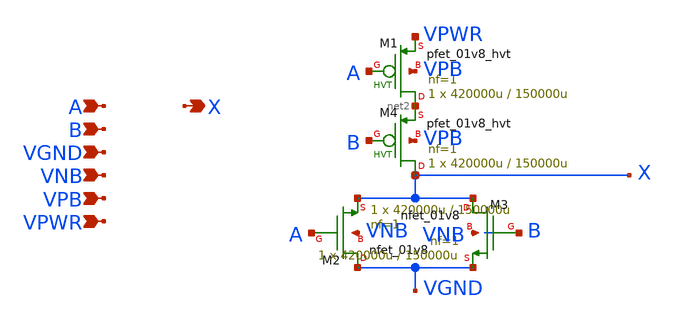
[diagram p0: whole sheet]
** sch_path: schematics/nor2/sky130_fd_sc_hd__nor2_1.sch
**.subckt sky130_fd_sc_hd__nor2_1 A X B VGND VNB VPB VPWR
*.ipin A
*.opin X
*.ipin B
*.ipin VGND
*.ipin VNB
*.ipin VPB
*.ipin VPWR
XM1 net2 A VPWR VPB sky130_fd_pr__pfet_01v8_hvt L=150000u W=420000u nf=1 ad='int((1 + 1)/2) * 420000u / 1 * 0.29'
+ as='int((1 + 2)/2) * 420000u / 1 * 0.29' pd='2*int((1 + 1)/2) * (420000u / 1 + 0.29)' ps='2*int((1 + 2)/2) * (420000u / 1 + 0.29)'
+ nrd='0.29 / 420000u ' nrs='0.29 / 420000u ' sa=0 sb=0 sd=0 mult=1 m=1
XM2 VGND A X VNB sky130_fd_pr__nfet_01v8 L=150000u W=420000u nf=1 ad='int((1 + 1)/2) * 420000u / 1 * 0.29'
+ as='int((1 + 2)/2) * 420000u / 1 * 0.29' pd='2*int((1 + 1)/2) * (420000u / 1 + 0.29)' ps='2*int((1 + 2)/2) * (420000u / 1 + 0.29)'
+ nrd='0.29 / 420000u ' nrs='0.29 / 420000u ' sa=0 sb=0 sd=0 mult=1 m=1
XM4 X B net2 VPB sky130_fd_pr__pfet_01v8_hvt L=150000u W=420000u nf=1 ad='int((1 + 1)/2) * 420000u / 1 * 0.29'
+ as='int((1 + 2)/2) * 420000u / 1 * 0.29' pd='2*int((1 + 1)/2) * (420000u / 1 + 0.29)' ps='2*int((1 + 2)/2) * (420000u / 1 + 0.29)'
+ nrd='0.29 / 420000u ' nrs='0.29 / 420000u ' sa=0 sb=0 sd=0 mult=1 m=1
XM3 X B VGND VNB sky130_fd_pr__nfet_01v8 L=150000u W=420000u nf=1 ad='int((1 + 1)/2) * 420000u / 1 * 0.29'
+ as='int((1 + 2)/2) * 420000u / 1 * 0.29' pd='2*int((1 + 1)/2) * (420000u / 1 + 0.29)' ps='2*int((1 + 2)/2) * (420000u / 1 + 0.29)'
+ nrd='0.29 / 420000u ' nrs='0.29 / 420000u ' sa=0 sb=0 sd=0 mult=1 m=1
**.ends
.end
